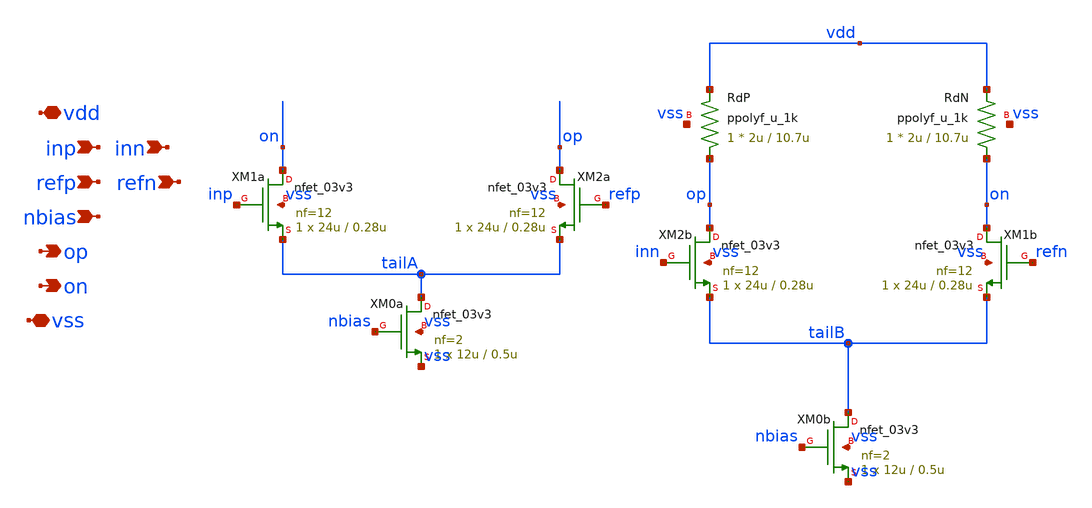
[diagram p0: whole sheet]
** sch_path: blocks/adc/comp-array/preamp.sch
**.subckt preamp vdd inp refp nbias op on vss inn refn
*.iopin vdd
*.ipin inp
*.ipin refp
*.ipin nbias
*.opin op
*.opin on
*.iopin vss
*.ipin inn
*.ipin refn
XM0b tailB nbias vss vss nfet_03v3 L=0.5u W=12u nf=2 ad='int((nf+1)/2) * W/nf * 0.18u' as='int((nf+2)/2) * W/nf * 0.18u'
+ pd='2*int((nf+1)/2) * (W/nf + 0.18u)' ps='2*int((nf+2)/2) * (W/nf + 0.18u)' nrd='0.18u / W' nrs='0.18u / W'
+ sa=0 sb=0 sd=0 m=1
XM2b op inn tailB vss nfet_03v3 L=0.28u W=24u nf=12 ad='int((nf+1)/2) * W/nf * 0.18u' as='int((nf+2)/2) * W/nf * 0.18u'
+ pd='2*int((nf+1)/2) * (W/nf + 0.18u)' ps='2*int((nf+2)/2) * (W/nf + 0.18u)' nrd='0.18u / W' nrs='0.18u / W'
+ sa=0 sb=0 sd=0 m=1
XM1b on refn tailB vss nfet_03v3 L=0.28u W=24u nf=12 ad='int((nf+1)/2) * W/nf * 0.18u' as='int((nf+2)/2) * W/nf * 0.18u'
+ pd='2*int((nf+1)/2) * (W/nf + 0.18u)' ps='2*int((nf+2)/2) * (W/nf + 0.18u)' nrd='0.18u / W' nrs='0.18u / W'
+ sa=0 sb=0 sd=0 m=1
XRdP op vdd vss ppolyf_u_1k r_width=2u r_length=10.7u m=1
XRdN on vdd vss ppolyf_u_1k r_width=2u r_length=10.7u m=1
XM0a tailA nbias vss vss nfet_03v3 L=0.5u W=12u nf=2 ad='int((nf+1)/2) * W/nf * 0.18u' as='int((nf+2)/2) * W/nf * 0.18u'
+ pd='2*int((nf+1)/2) * (W/nf + 0.18u)' ps='2*int((nf+2)/2) * (W/nf + 0.18u)' nrd='0.18u / W' nrs='0.18u / W'
+ sa=0 sb=0 sd=0 m=1
XM1a on inp tailA vss nfet_03v3 L=0.28u W=24u nf=12 ad='int((nf+1)/2) * W/nf * 0.18u' as='int((nf+2)/2) * W/nf * 0.18u'
+ pd='2*int((nf+1)/2) * (W/nf + 0.18u)' ps='2*int((nf+2)/2) * (W/nf + 0.18u)' nrd='0.18u / W' nrs='0.18u / W'
+ sa=0 sb=0 sd=0 m=1
XM2a op refp tailA vss nfet_03v3 L=0.28u W=24u nf=12 ad='int((nf+1)/2) * W/nf * 0.18u' as='int((nf+2)/2) * W/nf * 0.18u'
+ pd='2*int((nf+1)/2) * (W/nf + 0.18u)' ps='2*int((nf+2)/2) * (W/nf + 0.18u)' nrd='0.18u / W' nrs='0.18u / W'
+ sa=0 sb=0 sd=0 m=1
**.ends
.end
